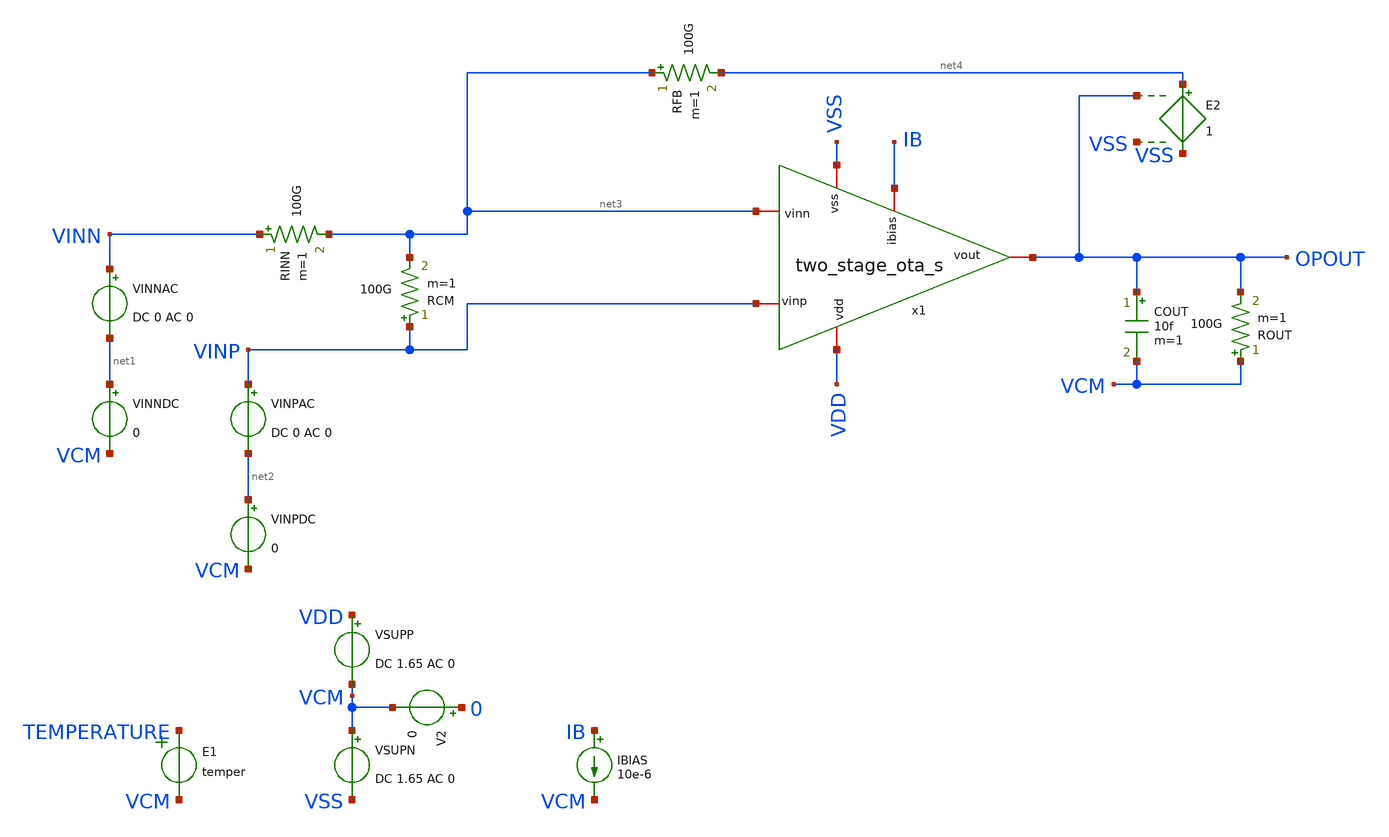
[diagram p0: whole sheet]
** sch_path: dependencies/pmu_ip/dependencies/OTA/OTA-main/testbenches/tw_stage_ota_s_tb_corner.sch
**.subckt tw_stage_ota_s_tb_corner
V2 0 VCM 0
E1 TEMPERATURE VCM VOL=' temper '
IBIAS IB VCM 10e-6
COUT OPOUT VCM 10f m=1
VINNDC net1 VCM 0
VINNAC VINN net1 DC 0 AC 0
VINPDC net2 VCM 0
VINPAC VINP net2 DC 0 AC 0
ROUT VCM OPOUT 100G m=1
VSUPP VDD VCM DC 1.65 AC 0
RFB net3 net4 100G m=1
RINN VINN net3 100G m=1
RCM VINP net3 100G m=1
VSUPN VCM VSS DC 1.65 AC 0
E2 net4 VSS OPOUT VSS 1
x1 VDD IB net3 VINP OPOUT VSS two_stage_ota_s
**** begin user architecture code


.csparam TB_ID=${::TB_ID}
.csparam MC_RUNS=${::MC_RUNS}
.csparam EXIT_NGSPICE=${::EXIT_NGSPICE}
.lib ${::IHP_MODELS}/sg13g2.lib ${::CORNER}



* this experimental option enables mos model bin
* selection based on W/NF instead of W
.option wnflag=0

.control
* option savecurrents

* dummy block for goto
if (1)
if TB_ID = 0
	goto TRAN_THD
end
if TB_ID = 1
	goto AC_OL
end
if TB_ID = 2
	goto AC_CMRR_PSRR
end
if TB_ID = 3
	goto TRAN_OUTRNG
end
if TB_ID = 4
	goto TRAN_CMINP
end
if TB_ID = 5
	goto TRAN_SLEW
end
if TB_ID = 6
	goto AC_INOISE
end
if TB_ID = 7
	goto TRAN_THD
end

* Helper Functions
******************
define aunif(nom, avar) (nom+avar*sunif(0))
define agauss(nom, avar, sig) (nom + avar / sig * sgauss (0))

****************************************
label AC_OL
save all
****************************************
if MC_RUNS = 0
	let olgain_1hz = vector(MC_RUNS+1)
	let pm = vector(MC_RUNS+1)
	let ugbw = vector(MC_RUNS+1)
	let f1_3db = vector(MC_RUNS+1)
	let f2_3db = vector(MC_RUNS+1)
	let run=0

	.include ac_ol_ops.inc

	set nobreak
	set width=300
	print col olgain_1hz, pm, ugbw, f1_3db, f2_3db > ac_ol.csv
else
	let olgain_1hz = vector(MC_RUNS)
	let pm = vector(MC_RUNS)
	let ugbw = vector(MC_RUNS)
	let f1_3db = vector(MC_RUNS)
	let f2_3db = vector(MC_RUNS)
	let run=0
	dowhile run < MC_RUNS
		echo MC-RUN: $&run

		.include ac_ol_ops.inc

 		reset
		let run = run + 1
	end
	set nobreak
	set width=300
	print olgain_1hz, pm, ugbw, f1_3db, f2_3db > ac_ol.csv
end
goto done

****************************************
label AC_CMRR_PSRR
save all
****************************************
if MC_RUNS = 0
	let cmrr_10Hz = vector(MC_RUNS+1)
	let cmrr_10MHz = vector(MC_RUNS+1)
	let psrr_p_10Hz = vector(MC_RUNS+1)
	let psrr_p_10MHz = vector(MC_RUNS+1)
	let psrr_n_10Hz = vector(MC_RUNS+1)
	let psrr_n_10MHz = vector(MC_RUNS+1)
	let run=0

	.include ac_cmrr_psrr_ops.inc

	set nobreak
	set width=300
	print col cmrr_10Hz, cmrr_10MHz, psrr_p_10Hz, psrr_p_10MHz, psrr_n_10Hz, psrr_n_10MHz >
+ ac_cmrr_psrr.csv
else
	let cmrr_10Hz = vector(MC_RUNS)
	let cmrr_10MHz = vector(MC_RUNS)
	let psrr_p_10Hz = vector(MC_RUNS)
	let psrr_p_10MHz = vector(MC_RUNS)
	let psrr_n_10Hz = vector(MC_RUNS)
	let psrr_n_10MHz = vector(MC_RUNS)
	let run=0
	dowhile run < MC_RUNS
		echo MC-RUN: $&run

		.include ac_cmrr_psrr_ops.inc

 		reset
		let run = run + 1
	end
	set nobreak
	set width=300
	print cmrr_10Hz, cmrr_10MHz, psrr_p_10Hz, psrr_p_10MHz, psrr_n_10Hz, psrr_n_10MHz >
+ ac_cmrr_psrr.csv
end
goto done

****************************************
label TRAN_OUTRNG
save all
****************************************
if MC_RUNS = 0
	let neg_out_comp = vector(MC_RUNS+1)
	let pos_out_comp = vector(MC_RUNS+1)
	let run=0

	.include tran_outrng_ops.inc

	set nobreak
	set width=300
	print col neg_out_comp, pos_out_comp > tran_outrng.csv
else
	let neg_out_comp = vector(MC_RUNS)
	let pos_out_comp = vector(MC_RUNS)
	let run=0
	dowhile run < MC_RUNS
		echo MC-RUN: $&run

		.include tran_outrng_ops.inc

 		reset
		let run = run + 1
	end
	set nobreak
	set width=300
	print neg_out_comp, pos_out_comp > tran_outrng.csv
end
goto done

****************************************
label TRAN_CMINP
save all
****************************************
if MC_RUNS = 0
	let pos_cm_bound = vector(MC_RUNS+1)
	let neg_cm_bound = vector(MC_RUNS+1)
	let run=0

	.include tran_cminp_ops.inc

	set nobreak
	set width=300
	print col pos_cm_bound, neg_cm_bound > tran_inprng.csv
else
	let pos_cm_bound = vector(MC_RUNS)
	let neg_cm_bound = vector(MC_RUNS)
	let run=0
	dowhile run < MC_RUNS
		echo MC-RUN: $&run

		.include tran_cminp_ops.inc

 		reset
		let run = run + 1
	end
	set nobreak
	set width=300
	print pos_cm_bound, neg_cm_bound > tran_inprng.csv
end
goto done

****************************************
label TRAN_SLEW
save all
****************************************
if MC_RUNS = 0
	let inp_offset = vector(MC_RUNS+1)
	let slew_pos = vector(MC_RUNS+1)
	let slew_neg = vector(MC_RUNS+1)
	let run=0

	.include tran_slew_ops.inc

	set nobreak
	set width=300
	print col inp_offset, slew_pos, slew_neg > tran_slew.csv
else
	let inp_offset = vector(MC_RUNS)
	let slew_pos = vector(MC_RUNS)
	let slew_neg = vector(MC_RUNS)
	let run=0
	dowhile run < MC_RUNS
		echo MC-RUN: $&run

		.include tran_slew_ops.inc

 		reset
		let run = run + 1
	end
	set nobreak
	set width=300
	print inp_offset, slew_pos, slew_neg > tran_slew.csv
end
goto done

****************************************
label AC_INOISE
****************************************
alter vsupp dc = 1.65
alter vsupp ac = 0
alter vsupn dc = 1.65
alter vsupn ac = 0
alter vinnac ac = 0
alter vinndc dc = 0
alter vinpac ac = 0
alter vinpdc dc = 0
alter rinn resistance = 100e12
alter rinn ac = 100e12
alter rcm resistance = 100e12
alter rcm ac = 100e12
alter rfb resistance = 0
alter rfb ac = 0.01

noise v(opout) vinpac dec 10 1 100e6 1
print noise2.onoise_total noise2.inoise_total
plot noise1.onoise_spectrum
plot noise1.inoise_spectrum
setplot noise1
write noise1_opout.raw all

* https://sourceforge.net/p/ngspice/discussion/120973/thread/2aa3e30f/ -- Holger Vogt
* script to read a specific y-value if x given
**********************************************
let f0 = vector(1)
let f1 = vector(1)
let n_f0 = vector(1)
let n_f1 = vector(1)
compose freq_list values 10 10e3
foreach freq_idx 0 1
	let freq = freq_list[$freq_idx]
	* find index where freqency is just above interesting value
	setplot noise1
	let nn = 0
	while frequency[nn] < freq
		let nn = nn + 1
	end
	* define vectors of frequncies and values just above and below
	* selected frequeny
	let fnn = frequency[nn]
	let nn1 = nn - 1
	let fnn1 = frequency[nn1]
	let snn = onoise_spectrum[nn]
	let snn1 = onoise_spectrum[nn1]
	*print vector values
	echo nn = $&nn  fnn = $&fnn  snn = $&snn
	echo nn1 = $&nn1  fnn1 = $&fnn1  snn1 = $&snn1
	*linear interpolation for exact frequency
	let newsnn = snn1 + (snn - snn1)/(fnn - fnn1)*(freq - fnn1)
	echo newfnn = $&freq  newsnn = $&newsnn
	if $freq_idx = 0
		let f0 = freq
		let n_f0 = newsnn
	end
	if $freq_idx = 1
		let f1 = freq
		let n_f1 = newsnn
	end
end
set nobreak
set width=300
set noprintscale
print col f0, n_f0, f1, n_f1 > ac_inoise.csv

goto done

****************************************
label TRAN_THD
*save all
****************************************
if MC_RUNS = 0
	let thd = vector(MC_RUNS+1)
	let run=0

	.include tran_thd_ops.inc

	set nobreak
	set width=300
	print col thd > tran_thd.csv
else
	let thd = vector(MC_RUNS)
	let run=0
	dowhile run < MC_RUNS
		echo MC-RUN: $&run

		reset

		.include tran_thd_ops.inc

		let run = run + 1
	end
	set nobreak
	set width=300
	print thd > tran_thd.csv
end
goto done

****************************************
label done
****************************************
if EXIT_NGSPICE > 0.0
	exit
end
end
.endc


**** end user architecture code
**.ends

* expanding   symbol:  two_stage_ota_s.sym # of pins=6
** sym_path: dependencies/pmu_ip/dependencies/OTA/OTA-main/testbenches/two_stage_ota_s.sym
** sch_path: dependencies/pmu_ip/dependencies/OTA/OTA-main/testbenches/two_stage_ota_s.sch
.subckt two_stage_ota_s vdd ibias vinn vinp vout vss
*.iopin ibias
*.iopin vdd
*.iopin vss
*.iopin vout
*.iopin vinp
*.iopin vinn
C1 net4 vout 350f m=1
R1 net3 net4 4k m=1
XM4 net3 net2 vss vss sg13_hv_nmos w=3u l=1u ng=1 m=1 mm_ok=1
XM3 net2 net2 vss vss sg13_hv_nmos w=3u l=1u ng=1 m=1 mm_ok=1
XM1 net3 vinp net1 vdd sg13_hv_pmos w=12u l=1u ng=1 m=2 mm_ok=1
XM2 net2 vinn net1 vdd sg13_hv_pmos w=12u l=1u ng=1 m=2 mm_ok=1
XM5 net1 ibias vdd vdd sg13_hv_pmos w=6u l=3u ng=1 m=2 mm_ok=1
XM7 vout ibias vdd vdd sg13_hv_pmos w=6u l=3u ng=1 m=8 mm_ok=1
XM8 ibias ibias vdd vdd sg13_hv_pmos w=6u l=3u ng=1 m=8 mm_ok=1
XM9 vout net3 vss vss sg13_hv_nmos w=12u l=1u ng=1 m=2 mm_ok=1
.ends

.end
